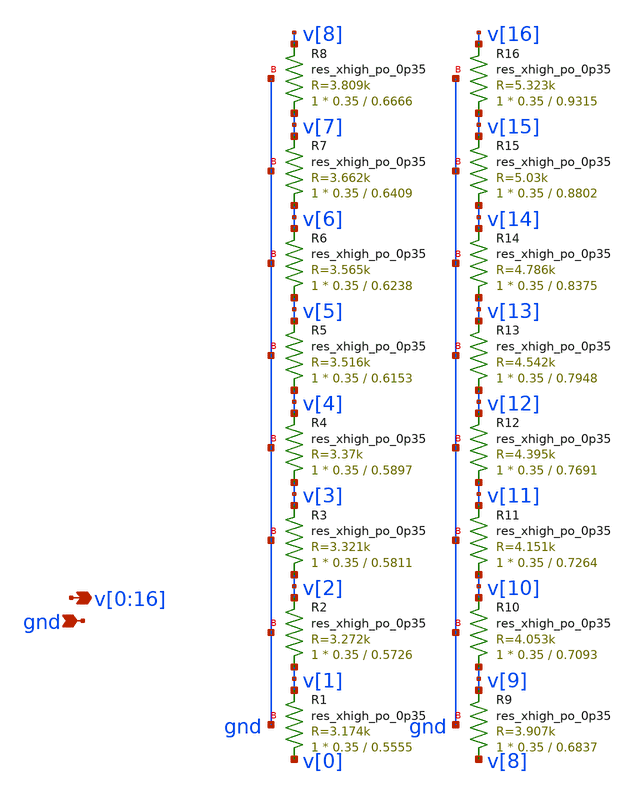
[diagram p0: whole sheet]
** sch_path: xschem/res_seg_3_v2.sch
**.subckt res_seg_3_v2
*+ v[0],v[1],v[2],v[3],v[4],v[5],v[6],v[7],v[8],v[9],v[10],v[11],v[12],v[13],v[14],v[15],v[16] gnd
*.opin v[0],v[1],v[2],v[3],v[4],v[5],v[6],v[7],v[8],v[9],v[10],v[11],v[12],v[13],v[14],v[15],v[16]
*.ipin gnd
XR1 v[0] v[1] gnd sky130_fd_pr__res_xhigh_po_0p35 L=0.5555 mult=1 m=1
XR2 v[1] v[2] gnd sky130_fd_pr__res_xhigh_po_0p35 L=0.5726 mult=1 m=1
XR3 v[2] v[3] gnd sky130_fd_pr__res_xhigh_po_0p35 L=0.5811 mult=1 m=1
XR4 v[3] v[4] gnd sky130_fd_pr__res_xhigh_po_0p35 L=0.5897 mult=1 m=1
XR5 v[4] v[5] gnd sky130_fd_pr__res_xhigh_po_0p35 L=0.6153 mult=1 m=1
XR6 v[5] v[6] gnd sky130_fd_pr__res_xhigh_po_0p35 L=0.6238 mult=1 m=1
XR7 v[6] v[7] gnd sky130_fd_pr__res_xhigh_po_0p35 L=0.6409 mult=1 m=1
XR8 v[7] v[8] gnd sky130_fd_pr__res_xhigh_po_0p35 L=0.6666 mult=1 m=1
XR9 v[8] v[9] gnd sky130_fd_pr__res_xhigh_po_0p35 L=0.6837 mult=1 m=1
XR10 v[9] v[10] gnd sky130_fd_pr__res_xhigh_po_0p35 L=0.7093 mult=1 m=1
XR11 v[10] v[11] gnd sky130_fd_pr__res_xhigh_po_0p35 L=0.7264 mult=1 m=1
XR12 v[11] v[12] gnd sky130_fd_pr__res_xhigh_po_0p35 L=0.7691 mult=1 m=1
XR13 v[12] v[13] gnd sky130_fd_pr__res_xhigh_po_0p35 L=0.7948 mult=1 m=1
XR14 v[13] v[14] gnd sky130_fd_pr__res_xhigh_po_0p35 L=0.8375 mult=1 m=1
XR15 v[14] v[15] gnd sky130_fd_pr__res_xhigh_po_0p35 L=0.8802 mult=1 m=1
XR16 v[15] v[16] gnd sky130_fd_pr__res_xhigh_po_0p35 L=0.9315 mult=1 m=1
**.ends
.end
